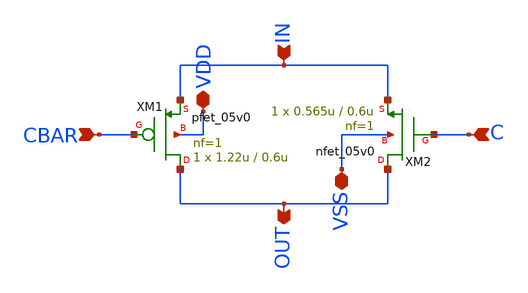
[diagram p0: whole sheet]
** sch_path: TGATE/TGATE.sch
**.subckt TGATE IN OUT CBAR C VDD VSS
*.ipin IN
*.opin OUT
*.ipin CBAR
*.ipin C
*.iopin VDD
*.iopin VSS
XM1 OUT CBAR IN VDD pfet_05v0 L=0.6u W=1.22u nf=1 ad='int((nf+1)/2) * W/nf * 0.18u' as='int((nf+2)/2) * W/nf * 0.18u'
+ pd='2*int((nf+1)/2) * (W/nf + 0.18u)' ps='2*int((nf+2)/2) * (W/nf + 0.18u)' nrd='0.18u / W' nrs='0.18u / W'
+ sa=0 sb=0 sd=0 m=1
XM2 OUT C IN VSS nfet_05v0 L=0.6u W=0.565u nf=1 ad='int((nf+1)/2) * W/nf * 0.18u' as='int((nf+2)/2) * W/nf * 0.18u'
+ pd='2*int((nf+1)/2) * (W/nf + 0.18u)' ps='2*int((nf+2)/2) * (W/nf + 0.18u)' nrd='0.18u / W' nrs='0.18u / W'
+ sa=0 sb=0 sd=0 m=1
**.ends
.end
